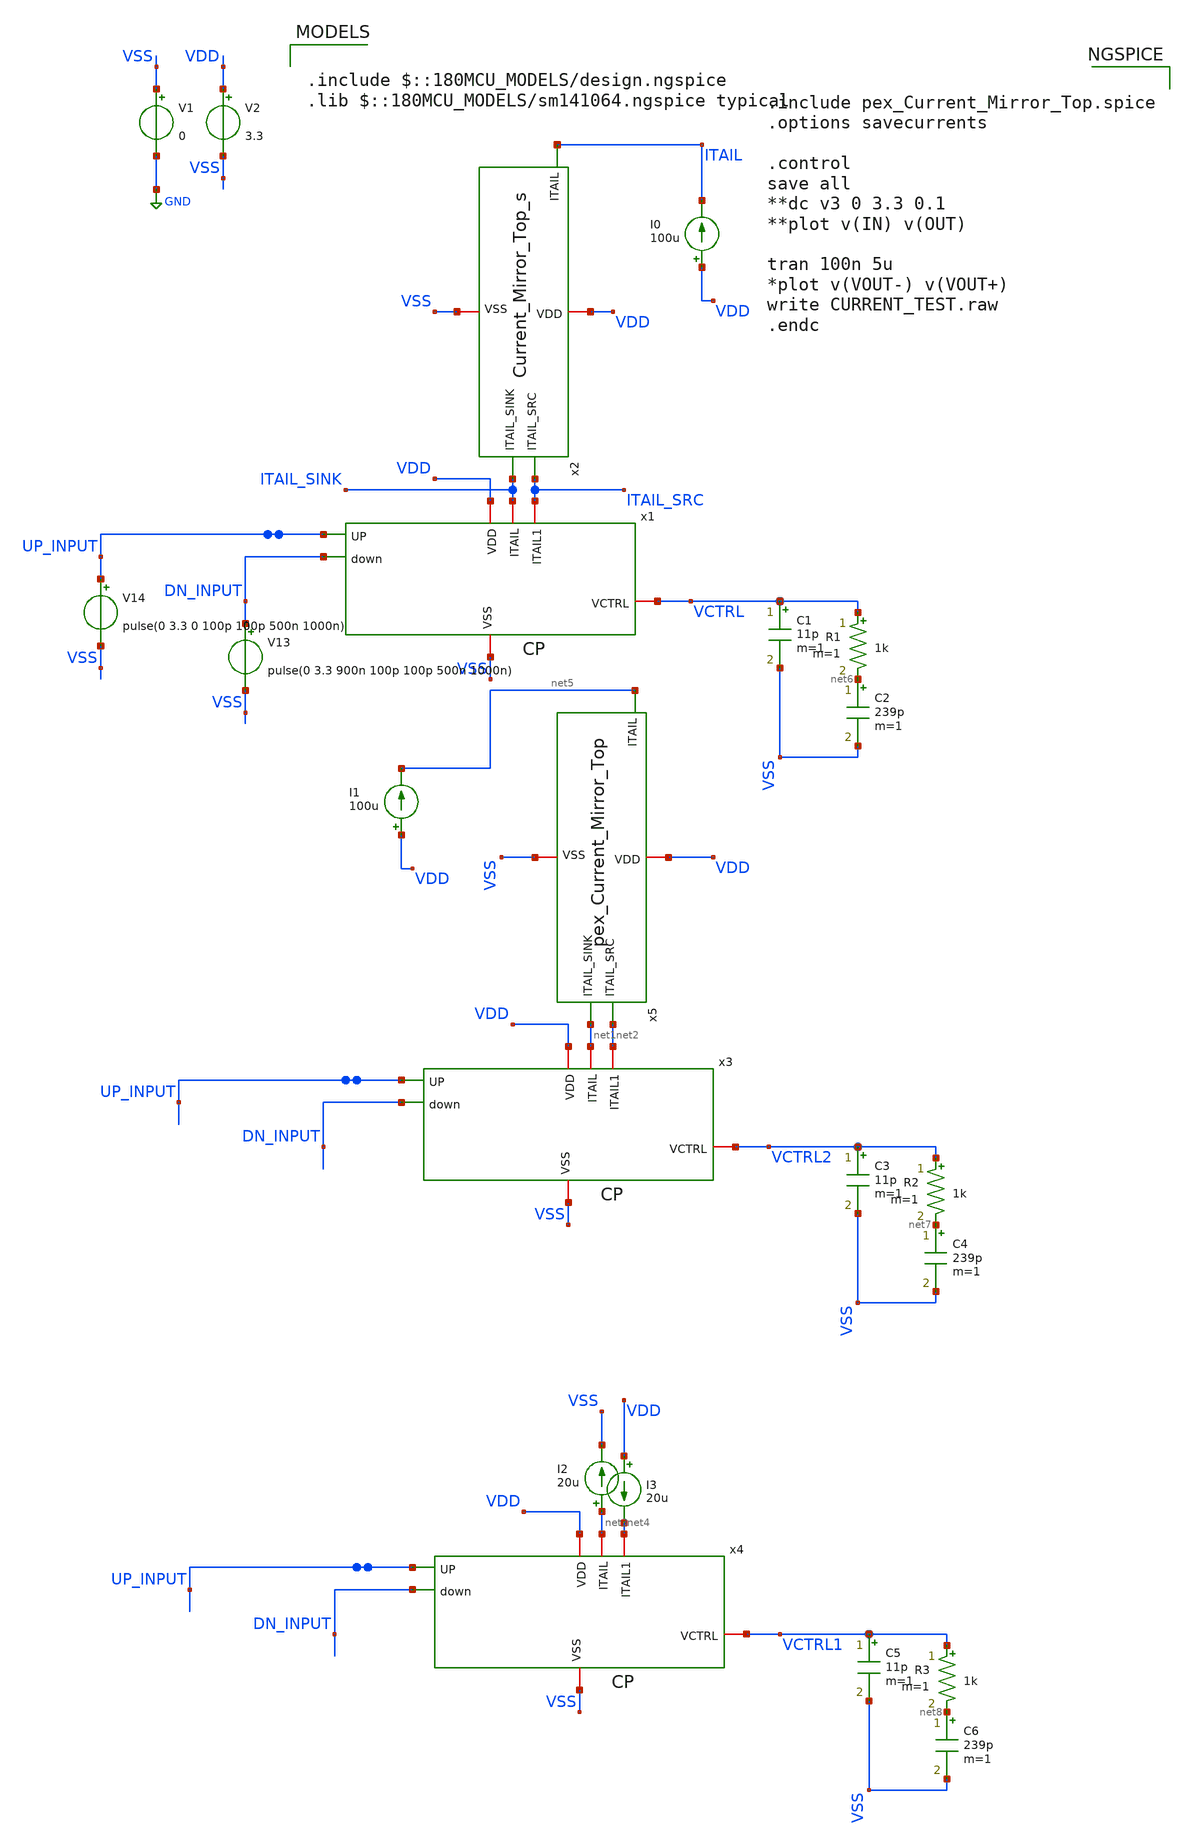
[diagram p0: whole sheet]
** sch_path: Clock_Generator_PAKISTAN_02/xschem/CURRENT_TEST.sch
**.subckt CURRENT_TEST
V1 VSS GND 0
V2 VDD VSS 3.3
x1 VDD ITAIL_SINK ITAIL_SRC VCTRL UP_INPUT DN_INPUT VSS CP
x2 VDD ITAIL ITAIL_SRC ITAIL_SINK VSS Current_Mirror_Top_s
I0 VDD ITAIL 100u
V13 DN_INPUT VSS pulse(0 3.3 900n 100p 100p 500n 1000n)
V14 UP_INPUT VSS pulse(0 3.3 0 100p 100p 500n 1000n)
C1 VCTRL VSS 11p m=1
C2 net6 VSS 239p m=1
R1 VCTRL net6 1k m=1
x3 VDD net1 net2 VCTRL2 UP_INPUT DN_INPUT VSS CP
C3 VCTRL2 VSS 11p m=1
C4 net7 VSS 239p m=1
R2 VCTRL2 net7 1k m=1
x4 VDD net3 net4 VCTRL1 UP_INPUT DN_INPUT VSS CP
C5 VCTRL1 VSS 11p m=1
C6 net8 VSS 239p m=1
R3 VCTRL1 net8 1k m=1
I1 VDD net5 100u
x5 VDD net5 net2 net1 VSS pex_Current_Mirror_Top
I2 net3 VSS 20u
I3 VDD net4 20u
**** begin user architecture code

.include $::180MCU_MODELS/design.ngspice
.lib $::180MCU_MODELS/sm141064.ngspice typical



.include pex_Current_Mirror_Top.spice
.options savecurrents

.control
save all
**dc v3 0 3.3 0.1
**plot v(IN) v(OUT)

tran 100n 5u
*plot v(VOUT-) v(VOUT+)
write CURRENT_TEST.raw
.endc


**** end user architecture code
**.ends
.GLOBAL GND
.end
